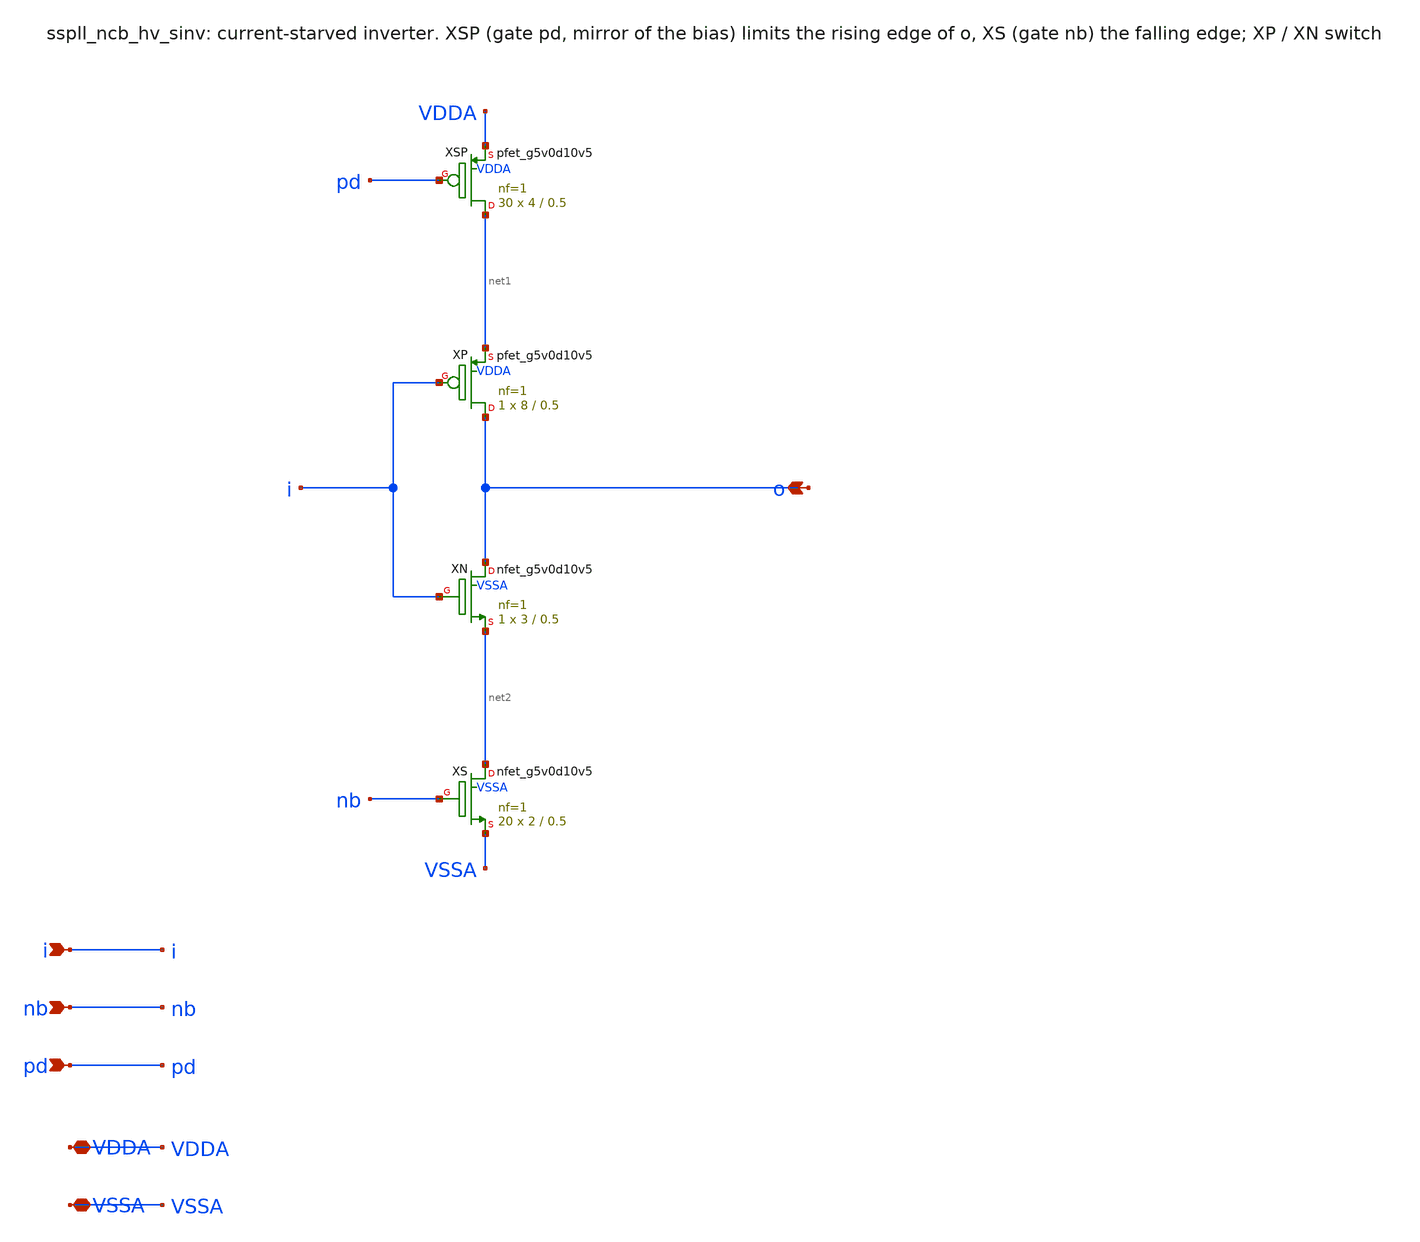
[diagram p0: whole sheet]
** sch_path: xschem/ncb_hv/sspll_ncb_hv_sinv.sch
**.subckt sspll_ncb_hv_sinv o i nb pd VDDA VSSA
*.opin o
*.ipin i
*.ipin nb
*.ipin pd
*.iopin VDDA
*.iopin VSSA
XXSP net1 pd VDDA VDDA sky130_fd_pr__pfet_g5v0d10v5 L=0.5 W=4 nf=1 ad='int((nf+1)/2) * W/nf * 0.29' as='int((nf+2)/2) * W/nf * 0.29'
+ pd='2*int((nf+1)/2) * (W/nf + 0.29)' ps='2*int((nf+2)/2) * (W/nf + 0.29)' nrd='0.29 / W' nrs='0.29 / W'
+ sa=0 sb=0 sd=0 mult=30 m=30
XXP o i net1 VDDA sky130_fd_pr__pfet_g5v0d10v5 L=0.5 W=8 nf=1 ad='int((nf+1)/2) * W/nf * 0.29' as='int((nf+2)/2) * W/nf * 0.29'
+ pd='2*int((nf+1)/2) * (W/nf + 0.29)' ps='2*int((nf+2)/2) * (W/nf + 0.29)' nrd='0.29 / W' nrs='0.29 / W'
+ sa=0 sb=0 sd=0 mult=1 m=1
XXN o i net2 VSSA sky130_fd_pr__nfet_g5v0d10v5 L=0.5 W=3 nf=1 ad='int((nf+1)/2) * W/nf * 0.29' as='int((nf+2)/2) * W/nf * 0.29'
+ pd='2*int((nf+1)/2) * (W/nf + 0.29)' ps='2*int((nf+2)/2) * (W/nf + 0.29)' nrd='0.29 / W' nrs='0.29 / W'
+ sa=0 sb=0 sd=0 mult=1 m=1
XXS net2 nb VSSA VSSA sky130_fd_pr__nfet_g5v0d10v5 L=0.5 W=2 nf=1 ad='int((nf+1)/2) * W/nf * 0.29' as='int((nf+2)/2) * W/nf * 0.29'
+ pd='2*int((nf+1)/2) * (W/nf + 0.29)' ps='2*int((nf+2)/2) * (W/nf + 0.29)' nrd='0.29 / W' nrs='0.29 / W'
+ sa=0 sb=0 sd=0 mult=20 m=20
**.ends
.end
